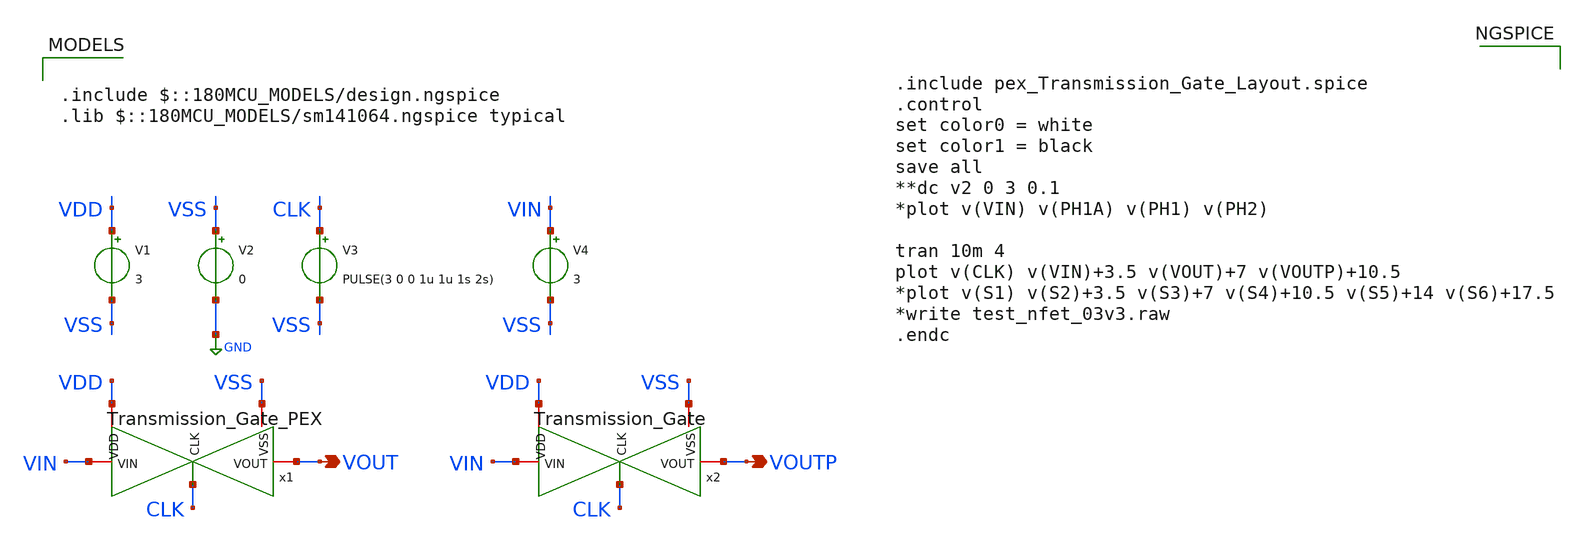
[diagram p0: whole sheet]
** sch_path: SCOP_INPUT_AND_MUX_PAKISTAN_03/Xschem/Logic_Gates/Transmission_Gate_TB.sch
**.subckt Transmission_Gate_TB VOUT VOUTP
*.opin VOUT
*.opin VOUTP
x2 VDD VSS CLK VOUTP VIN Transmission_Gate
V1 VDD VSS 3
V2 VSS GND 0
V3 CLK VSS PULSE(3 0 0 1u 1u 1s 2s)
V4 VIN VSS 3
x1 VDD VSS CLK VOUT VIN Transmission_Gate_PEX
**** begin user architecture code

.include $::180MCU_MODELS/design.ngspice
.lib $::180MCU_MODELS/sm141064.ngspice typical



.include pex_Transmission_Gate_Layout.spice
.control
set color0 = white
set color1 = black
save all
**dc v2 0 3 0.1
*plot v(VIN) v(PH1A) v(PH1) v(PH2)

tran 10m 4
plot v(CLK) v(VIN)+3.5 v(VOUT)+7 v(VOUTP)+10.5
*plot v(S1) v(S2)+3.5 v(S3)+7 v(S4)+10.5 v(S5)+14 v(S6)+17.5
*write test_nfet_03v3.raw
.endc


**** end user architecture code
**.ends

* expanding   symbol:  Transmission_Gate.sym # of pins=5
** sym_path: SCOP_INPUT_AND_MUX_PAKISTAN_03/Xschem/Logic_Gates/Transmission_Gate.sym
** sch_path: SCOP_INPUT_AND_MUX_PAKISTAN_03/Xschem/Logic_Gates/Transmission_Gate.sch
.subckt Transmission_Gate VDD VSS CLK VOUT VIN
*.iopin VIN
*.iopin VOUT
*.ipin CLK
*.iopin VDD
*.iopin VSS
XM1 VOUT CLK_B VIN VDD pfet_03v3 L=0.28u W=60u nf=1 ad='int((nf+1)/2) * W/nf * 0.18u' as='int((nf+2)/2) * W/nf * 0.18u'
+ pd='2*int((nf+1)/2) * (W/nf + 0.18u)' ps='2*int((nf+2)/2) * (W/nf + 0.18u)' nrd='0.18u / W' nrs='0.18u / W'
+ sa=0 sb=0 sd=0 m=1
XM2 VOUT CLK VIN VSS nfet_03v3 L=0.28u W=30u nf=1 ad='int((nf+1)/2) * W/nf * 0.18u' as='int((nf+2)/2) * W/nf * 0.18u'
+ pd='2*int((nf+1)/2) * (W/nf + 0.18u)' ps='2*int((nf+2)/2) * (W/nf + 0.18u)' nrd='0.18u / W' nrs='0.18u / W'
+ sa=0 sb=0 sd=0 m=1
XM3 CLK_B CLK VDD VDD pfet_03v3 L=0.28u W=7.5u nf=1 ad='int((nf+1)/2) * W/nf * 0.18u' as='int((nf+2)/2) * W/nf * 0.18u'
+ pd='2*int((nf+1)/2) * (W/nf + 0.18u)' ps='2*int((nf+2)/2) * (W/nf + 0.18u)' nrd='0.18u / W' nrs='0.18u / W'
+ sa=0 sb=0 sd=0 m=1
XM4 CLK_B CLK VSS VSS nfet_03v3 L=0.28u W=3.75u nf=1 ad='int((nf+1)/2) * W/nf * 0.18u' as='int((nf+2)/2) * W/nf * 0.18u'
+ pd='2*int((nf+1)/2) * (W/nf + 0.18u)' ps='2*int((nf+2)/2) * (W/nf + 0.18u)' nrd='0.18u / W' nrs='0.18u / W'
+ sa=0 sb=0 sd=0 m=1
.ends

.GLOBAL GND
.end
